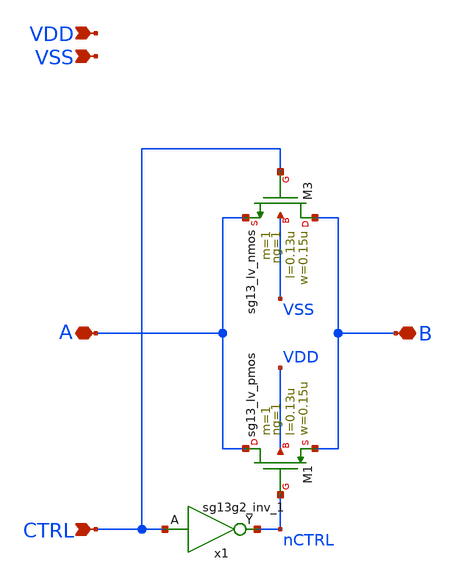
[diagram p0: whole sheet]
** sch_path: ngspice_cosim_tgate/tgate.sch
**.subckt tgate CTRL B A VDD VSS
*.ipin CTRL
*.iopin B
*.iopin A
*.ipin VDD
*.ipin VSS
x1 nCTRL CTRL VDD VSS sg13g2_inv_1
XM3 B CTRL A VSS sg13_lv_nmos w=0.15u l=0.13u ng=1 m=1 mm_ok=1
XM1 A nCTRL B VDD sg13_lv_pmos w=0.15u l=0.13u ng=1 m=1 mm_ok=1
**.ends

* expanding   symbol:  sg13g2_stdcells/sg13g2_inv_1.sym # of pins=2
** sym_path: sg13g2_stdcells/sg13g2_inv_1.sym
** sch_path: sg13g2_stdcells/sg13g2_inv_1.sch
.subckt sg13g2_inv_1 Y A VDD VSS
*.opin Y
*.ipin A
*.iopin VDD
*.iopin VSS
XM1 Y A VSS VSS sg13_lv_nmos w=740.00n l=130.00n ng=1 m=1 mm_ok=1
XM2 Y A VDD VDD sg13_lv_pmos w=1.12u l=130.00n ng=1 m=1 mm_ok=1
.ends

.end
